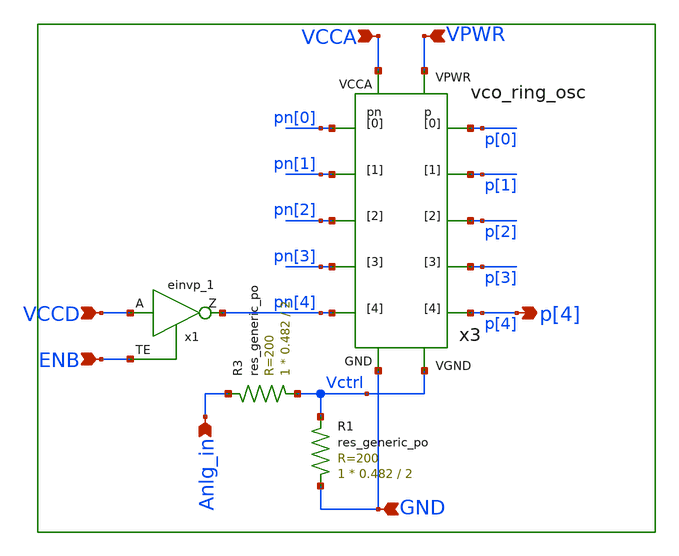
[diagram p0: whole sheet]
** sch_path: xschem/lib_vco/vco.sch
**.subckt vco Anlg_in p[4] VCCA VCCD ENB VPWR GND
*.ipin Anlg_in
*.opin p[4]
*.ipin VCCA
*.ipin VCCD
*.ipin ENB
*.ipin VPWR
*.ipin GND
x1 VCCD ENB GND GND VCCD VCCD pn[4] sky130_fd_sc_hd__einvp_1
XR3 Vctrl Anlg_in sky130_fd_pr__res_generic_po W=0.482 L=2 m=1
XR1 GND Vctrl sky130_fd_pr__res_generic_po W=0.482 L=2 m=1
x3 VCCA GND Vctrl VPWR p[0] p[1] p[2] p[3] p[4] pn[0] pn[1] pn[2] pn[3] pn[4] vco_ring_osc
**.ends
.end
